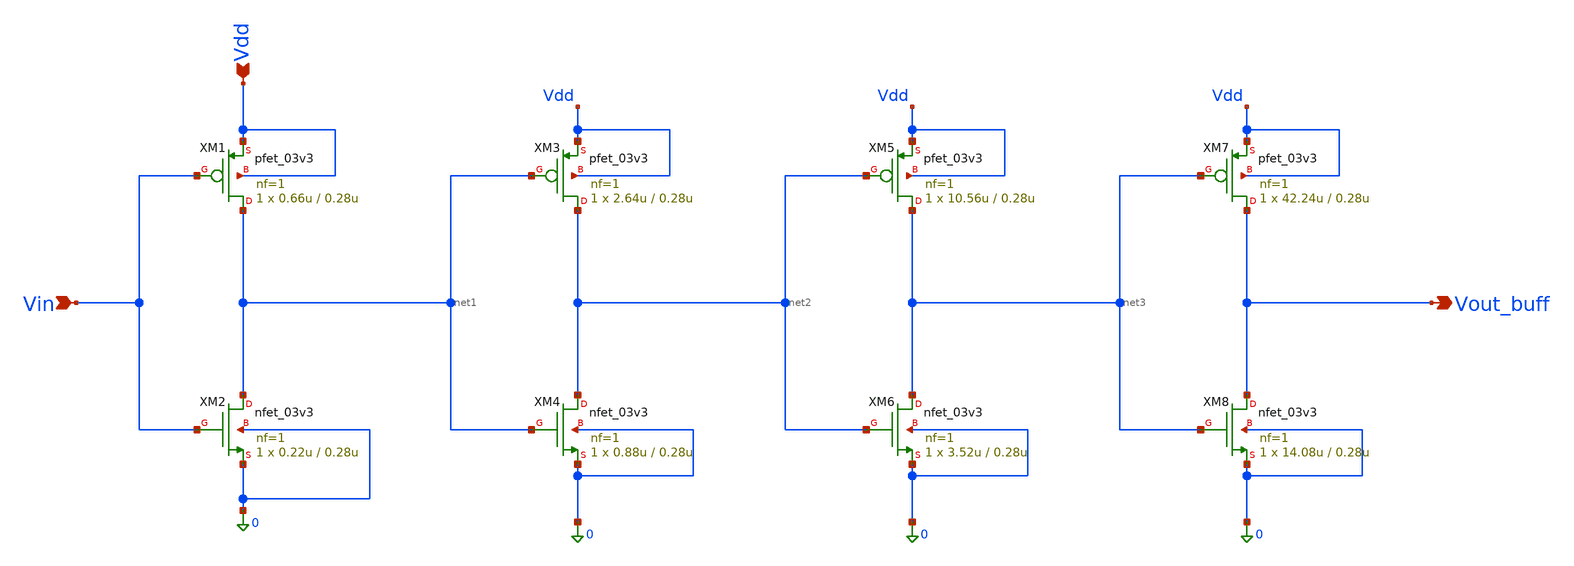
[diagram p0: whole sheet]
** sch_path: blocks/adc/lvds/buffer.sch
**.subckt buffer Vdd Vin Vout_buff
*.ipin Vdd
*.ipin Vin
*.opin Vout_buff
XM1 net1 Vin Vdd Vdd pfet_03v3 L=0.28u W=0.66u nf=1 ad='int((nf+1)/2) * W/nf * 0.18u' as='int((nf+2)/2) * W/nf * 0.18u'
+ pd='2*int((nf+1)/2) * (W/nf + 0.18u)' ps='2*int((nf+2)/2) * (W/nf + 0.18u)' nrd='0.18u / W' nrs='0.18u / W'
+ sa=0 sb=0 sd=0 m=1
XM2 net1 Vin 0 0 nfet_03v3 L=0.28u W=0.22u nf=1 ad='int((nf+1)/2) * W/nf * 0.18u' as='int((nf+2)/2) * W/nf * 0.18u'
+ pd='2*int((nf+1)/2) * (W/nf + 0.18u)' ps='2*int((nf+2)/2) * (W/nf + 0.18u)' nrd='0.18u / W' nrs='0.18u / W'
+ sa=0 sb=0 sd=0 m=1
XM3 net2 net1 Vdd Vdd pfet_03v3 L=0.28u W=2.64u nf=1 ad='int((nf+1)/2) * W/nf * 0.18u' as='int((nf+2)/2) * W/nf * 0.18u'
+ pd='2*int((nf+1)/2) * (W/nf + 0.18u)' ps='2*int((nf+2)/2) * (W/nf + 0.18u)' nrd='0.18u / W' nrs='0.18u / W'
+ sa=0 sb=0 sd=0 m=1
XM4 net2 net1 0 0 nfet_03v3 L=0.28u W=0.88u nf=1 ad='int((nf+1)/2) * W/nf * 0.18u' as='int((nf+2)/2) * W/nf * 0.18u'
+ pd='2*int((nf+1)/2) * (W/nf + 0.18u)' ps='2*int((nf+2)/2) * (W/nf + 0.18u)' nrd='0.18u / W' nrs='0.18u / W'
+ sa=0 sb=0 sd=0 m=1
XM5 net3 net2 Vdd Vdd pfet_03v3 L=0.28u W=10.56u nf=1 ad='int((nf+1)/2) * W/nf * 0.18u' as='int((nf+2)/2) * W/nf * 0.18u'
+ pd='2*int((nf+1)/2) * (W/nf + 0.18u)' ps='2*int((nf+2)/2) * (W/nf + 0.18u)' nrd='0.18u / W' nrs='0.18u / W'
+ sa=0 sb=0 sd=0 m=1
XM6 net3 net2 0 0 nfet_03v3 L=0.28u W=3.52u nf=1 ad='int((nf+1)/2) * W/nf * 0.18u' as='int((nf+2)/2) * W/nf * 0.18u'
+ pd='2*int((nf+1)/2) * (W/nf + 0.18u)' ps='2*int((nf+2)/2) * (W/nf + 0.18u)' nrd='0.18u / W' nrs='0.18u / W'
+ sa=0 sb=0 sd=0 m=1
XM7 Vout_buff net3 Vdd Vdd pfet_03v3 L=0.28u W=42.24u nf=1 ad='int((nf+1)/2) * W/nf * 0.18u' as='int((nf+2)/2) * W/nf * 0.18u'
+ pd='2*int((nf+1)/2) * (W/nf + 0.18u)' ps='2*int((nf+2)/2) * (W/nf + 0.18u)' nrd='0.18u / W' nrs='0.18u / W'
+ sa=0 sb=0 sd=0 m=1
XM8 Vout_buff net3 0 0 nfet_03v3 L=0.28u W=14.08u nf=1 ad='int((nf+1)/2) * W/nf * 0.18u' as='int((nf+2)/2) * W/nf * 0.18u'
+ pd='2*int((nf+1)/2) * (W/nf + 0.18u)' ps='2*int((nf+2)/2) * (W/nf + 0.18u)' nrd='0.18u / W' nrs='0.18u / W'
+ sa=0 sb=0 sd=0 m=1
**.ends
.end
